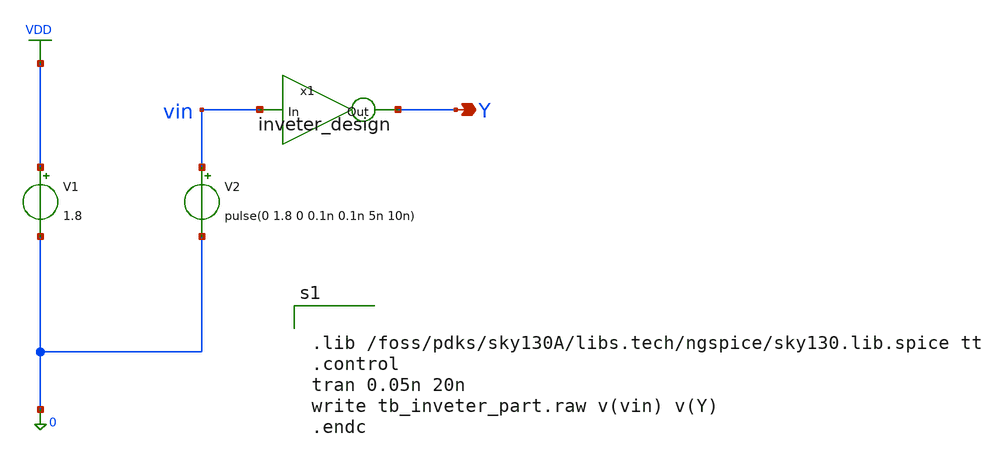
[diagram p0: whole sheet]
** sch_path: cells/full_adder_tg/xschem/tb_inveter_part.sch
**.subckt tb_inveter_part Y
*.opin Y
V1 VDD 0 1.8
V2 vin 0 pulse(0 1.8 0 0.1n 0.1n 5n 10n)
x1 Y vin inveter_design
**** begin user architecture code


.lib /foss/pdks/sky130A/libs.tech/ngspice/sky130.lib.spice tt
.control
tran 0.05n 20n
write tb_inveter_part.raw v(vin) v(Y)
.endc

**** end user architecture code
**.ends

* expanding   symbol:  ./inveter_design.sym # of pins=2
** sym_path: cells/full_adder_tg/xschem/inveter_design.sym
** sch_path: cells/full_adder_tg/xschem/inveter_design.sch
.subckt inveter_design Out In
*.ipin In
*.opin Out
XMNMOS Out In 0 0 sky130_fd_pr__nfet_01v8 L=0.15 W=2 nf=1 ad='int((1 + 1)/2) * 2 / 1 * 0.29' as='int((1 + 2)/2) * 2 / 1 * 0.29'
+ pd='2*int((1 + 1)/2) * (2 / 1 + 0.29)' ps='2*int((1 + 2)/2) * (2 / 1 + 0.29)' nrd='0.29 / 2 ' nrs='0.29 / 2 '
+ sa=0 sb=0 sd=0 mult=1 m=1
XMPMOS Out In VDD VDD sky130_fd_pr__pfet_01v8 L=0.15 W=5 nf=1 ad='int((1 + 1)/2) * 5 / 1 * 0.29' as='int((1 + 2)/2) * 5 / 1 * 0.29'
+ pd='2*int((1 + 1)/2) * (5 / 1 + 0.29)' ps='2*int((1 + 2)/2) * (5 / 1 + 0.29)' nrd='0.29 / 5 ' nrs='0.29 / 5 '
+ sa=0 sb=0 sd=0 mult=1 m=1
.ends

.GLOBAL VDD
.end
